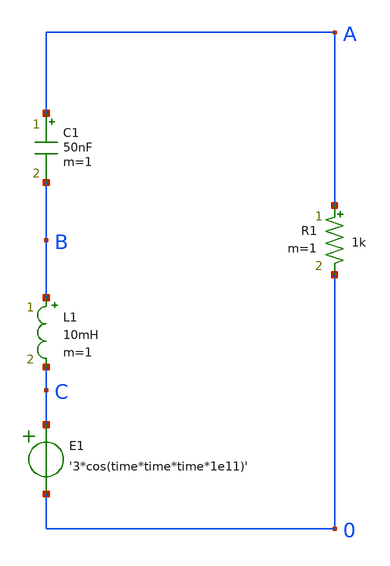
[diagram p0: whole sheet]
** sch_path: projects/tutorial/xschem_ngspice/rlc.sch
**.subckt rlc
R1 A 0 1k m=1
L1 B C 10mH m=1
E1 C 0 VOL=' '3*cos(time*time*time*1e11)' '
C1 A B 50nF m=1
**** begin user architecture code


.tran 10n 2000u uic
.save all


**** end user architecture code
**.ends
.end
